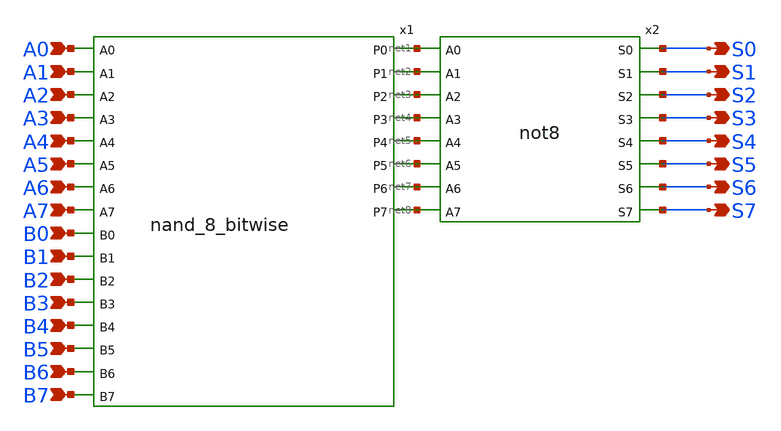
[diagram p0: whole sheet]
** sch_path: design/xschem/AND8/AND.sch
**.subckt AND S6 S7 S3 S4 S5 S0 S1 S2 A0 A1 B1 A2 B2 A3 B3 A4 B4 A5 B5 A6 B6 A7 B7 B0
*.opin S6
*.opin S7
*.opin S3
*.opin S4
*.opin S5
*.opin S0
*.opin S1
*.opin S2
*.ipin A0
*.ipin A1
*.ipin B1
*.ipin A2
*.ipin B2
*.ipin A3
*.ipin B3
*.ipin A4
*.ipin B4
*.ipin A5
*.ipin B5
*.ipin A6
*.ipin B6
*.ipin A7
*.ipin B7
*.ipin B0
x1 A0 A1 A2 A3 A4 A5 A6 A7 B0 B1 B2 B3 B4 B5 B6 B7 net1 net2 net3 net4 net5 net6 net7 net8
+ nand_8_bitwise
x2 net1 net2 net3 net4 net5 net6 net7 net8 S0 S1 S2 S3 S4 S5 S6 S7 VSS VDD not8
**.ends

* expanding   symbol:  NAND/nand_8_bitwise.sym # of pins=24
** sym_path: design/xschem/NAND/nand_8_bitwise.sym
** sch_path: design/xschem/NAND/nand_8_bitwise.sch
.subckt nand_8_bitwise A0 A1 A2 A3 A4 A5 A6 A7 B0 B1 B2 B3 B4 B5 B6 B7 P0 P1 P2 P3 P4 P5 P6 P7
*.ipin B7
*.ipin B5
*.ipin B6
*.ipin B4
*.ipin B3
*.ipin B2
*.ipin B1
*.ipin B0
*.opin P7
*.opin P6
*.opin P5
*.opin P4
*.opin P3
*.opin P2
*.opin P1
*.opin P0
*.ipin A7
*.ipin A5
*.ipin A6
*.ipin A4
*.ipin A3
*.ipin A2
*.ipin A1
*.ipin A0
x1 B7 A7 VSS VDD P7 nand2
x2 B6 A6 VSS VDD P6 nand2
x3 B5 A5 VSS VDD P5 nand2
x4 B4 A4 VSS VDD P4 nand2
x5 B3 A3 VSS VDD P3 nand2
x6 B2 A2 VSS VDD P2 nand2
x7 B1 A1 VSS VDD P1 nand2
x8 B0 A0 VSS VDD P0 nand2
.ends


* expanding   symbol:  NOT/not8.sym # of pins=16
** sym_path: design/xschem/NOT/not8.sym
** sch_path: design/xschem/NOT/not8.sch
.subckt not8 A0 A1 A2 A3 A4 A5 A6 A7 S0 S1 S2 S3 S4 S5 S6 S7 VSS VDD
*.ipin A7
*.ipin A5
*.ipin A6
*.ipin A4
*.ipin A3
*.ipin A2
*.ipin A1
*.ipin A0
*.opin S7
*.opin S6
*.opin S5
*.opin S4
*.opin S3
*.opin S2
*.opin S1
*.opin S0
x1 A3 VSS VDD S3 inv
x2 A2 VSS VDD S2 inv
x3 A1 VSS VDD S1 inv
x4 A4 VSS VDD S4 inv
x5 A5 VSS VDD S5 inv
x6 A6 VSS VDD S6 inv
x7 A0 VSS VDD S0 inv
x9 A7 VSS VDD S7 inv
.ends


* expanding   symbol:  NAND/nand2.sym # of pins=3
** sym_path: design/xschem/NAND/nand2.sym
** sch_path: design/xschem/NAND/nand2.sch
.subckt nand2 A B VSS VDD Y
*.ipin A
*.opin Y
*.ipin B
XM1 Y A VDD VDD sky130_fd_pr__pfet_01v8 L=0.15 W=3.2 nf=1 ad='int((nf+1)/2) * W/nf * 0.29' as='int((nf+2)/2) * W/nf * 0.29'
+ pd='2*int((nf+1)/2) * (W/nf + 0.29)' ps='2*int((nf+2)/2) * (W/nf + 0.29)' nrd='0.29 / W' nrs='0.29 / W'
+ sa=0 sb=0 sd=0 mult=1 m=1
XM2 Y A net1 net1 sky130_fd_pr__nfet_01v8 L=0.15 W=2 nf=1 ad='int((nf+1)/2) * W/nf * 0.29' as='int((nf+2)/2) * W/nf * 0.29'
+ pd='2*int((nf+1)/2) * (W/nf + 0.29)' ps='2*int((nf+2)/2) * (W/nf + 0.29)' nrd='0.29 / W' nrs='0.29 / W'
+ sa=0 sb=0 sd=0 mult=1 m=1
XM3 net1 B VSS VSS sky130_fd_pr__nfet_01v8 L=0.15 W=2 nf=1 ad='int((nf+1)/2) * W/nf * 0.29' as='int((nf+2)/2) * W/nf * 0.29'
+ pd='2*int((nf+1)/2) * (W/nf + 0.29)' ps='2*int((nf+2)/2) * (W/nf + 0.29)' nrd='0.29 / W' nrs='0.29 / W'
+ sa=0 sb=0 sd=0 mult=1 m=1
XM4 Y B VDD VDD sky130_fd_pr__pfet_01v8 L=0.15 W=3.2 nf=1 ad='int((nf+1)/2) * W/nf * 0.29' as='int((nf+2)/2) * W/nf * 0.29'
+ pd='2*int((nf+1)/2) * (W/nf + 0.29)' ps='2*int((nf+2)/2) * (W/nf + 0.29)' nrd='0.29 / W' nrs='0.29 / W'
+ sa=0 sb=0 sd=0 mult=1 m=1
.ends


* expanding   symbol:  INV/inv.sym # of pins=2
** sym_path: design/xschem/INV/inv.sym
** sch_path: design/xschem/INV/inv.sch
.subckt inv A VSS VDD Y
*.ipin A
*.opin Y
XM2 Y A VSS GND sky130_fd_pr__nfet_01v8 L=0.15 W=1 nf=1 ad='int((nf+1)/2) * W/nf * 0.29' as='int((nf+2)/2) * W/nf * 0.29'
+ pd='2*int((nf+1)/2) * (W/nf + 0.29)' ps='2*int((nf+2)/2) * (W/nf + 0.29)' nrd='0.29 / W' nrs='0.29 / W'
+ sa=0 sb=0 sd=0 mult=1 m=1
XM1 Y A VDD VDD sky130_fd_pr__pfet_01v8 L=0.15 W=3.21 nf=1 ad='int((nf+1)/2) * W/nf * 0.29' as='int((nf+2)/2) * W/nf * 0.29'
+ pd='2*int((nf+1)/2) * (W/nf + 0.29)' ps='2*int((nf+2)/2) * (W/nf + 0.29)' nrd='0.29 / W' nrs='0.29 / W'
+ sa=0 sb=0 sd=0 mult=1 m=1
.ends

.end
